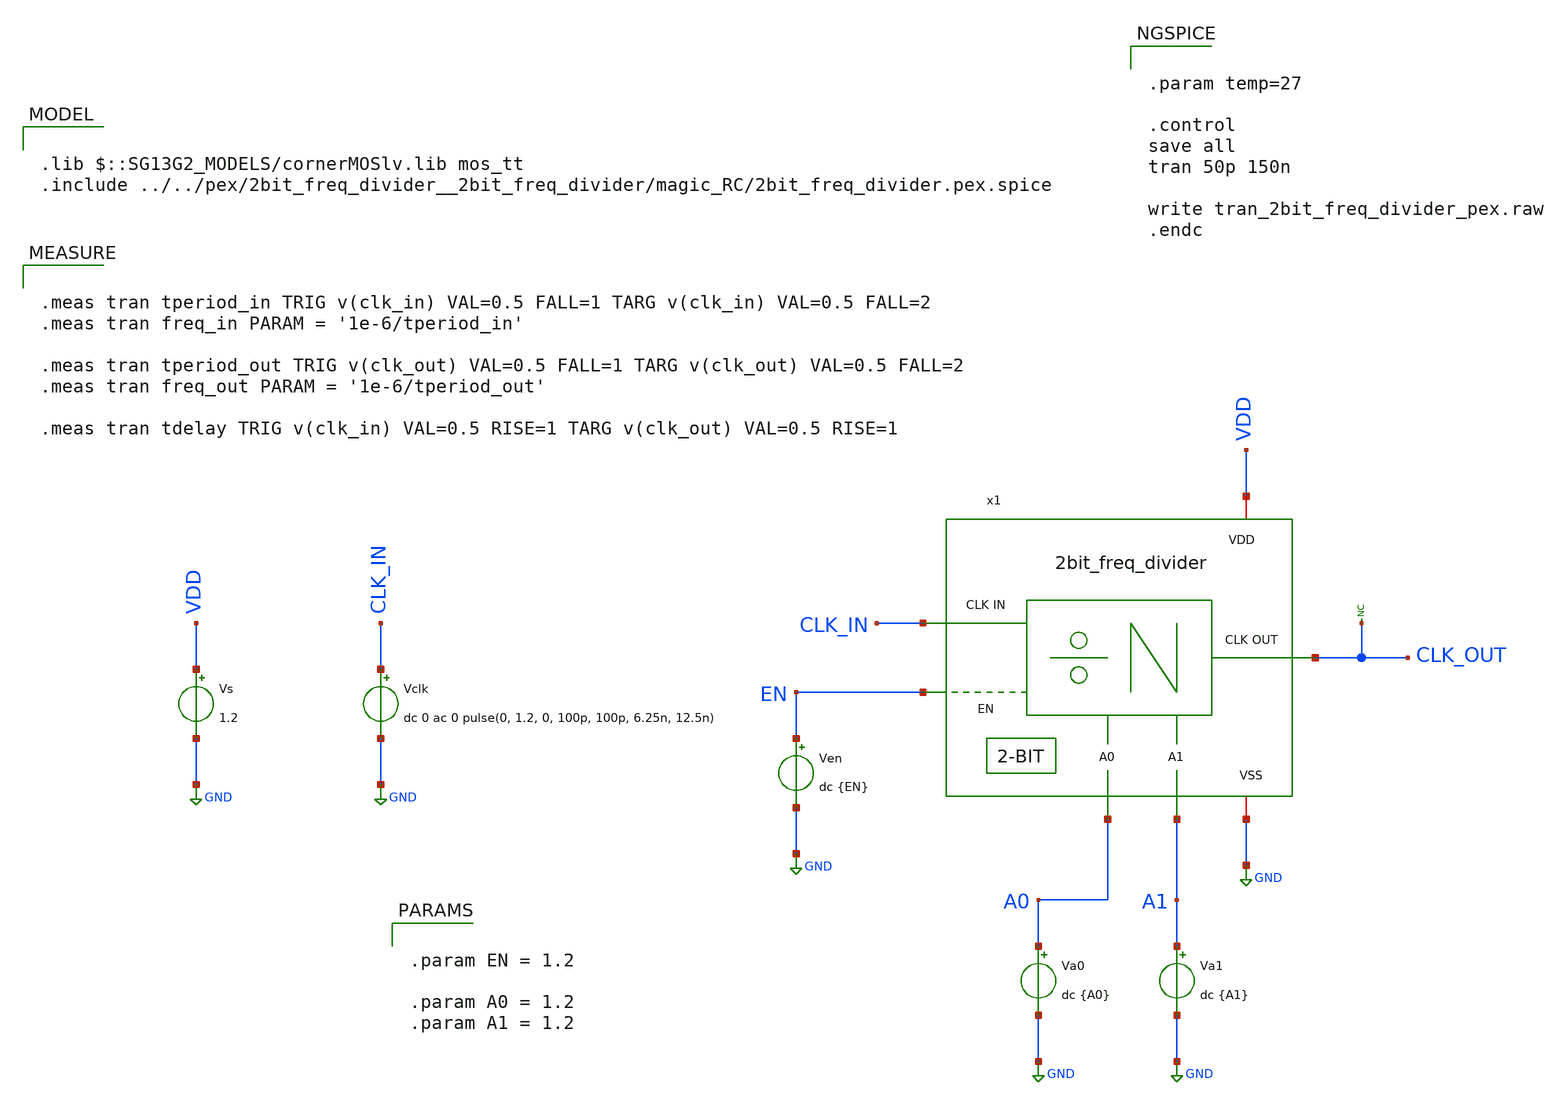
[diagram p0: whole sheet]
** sch_path: Combined_Design/design_data/xschem/2bit_freq_divider_pex_tb.sch

.lib $::SG13G2_MODELS/cornerMOSlv.lib mos_tt
.include ../../pex/2bit_freq_divider__2bit_freq_divider/magic_RC/2bit_freq_divider.pex.spice

**.subckt 2bit_freq_divider_pex_tb
Vs VDD GND 1.2
Vclk CLK_IN GND dc 0 ac 0 pulse(0, 1.2, 0, 100p, 100p, 6.25n, 12.5n)
* noconn CLK_OUT
Ven EN GND dc {EN}
Va0 A0 GND dc {A0}
Va1 A1 GND dc {A1}
x1 VDD GND A0 CLK_OUT CLK_IN EN A1 2bit_freq_divider
**** begin user architecture code


.meas tran tperiod_in TRIG v(clk_in) VAL=0.5 FALL=1 TARG v(clk_in) VAL=0.5 FALL=2
.meas tran freq_in PARAM = '1e-6/tperiod_in'

.meas tran tperiod_out TRIG v(clk_out) VAL=0.5 FALL=1 TARG v(clk_out) VAL=0.5 FALL=2
.meas tran freq_out PARAM = '1e-6/tperiod_out'

.meas tran tdelay TRIG v(clk_in) VAL=0.5 RISE=1 TARG v(clk_out) VAL=0.5 RISE=1




.param EN = 1.2

.param A0 = 1.2
.param A1 = 1.2




.param temp=27

.control
save all
tran 50p 150n

write tran_2bit_freq_divider_pex.raw
.endc


**** end user architecture code
**.ends
.GLOBAL GND
.end
